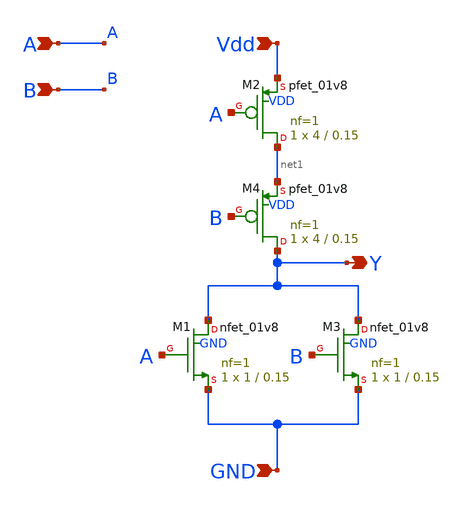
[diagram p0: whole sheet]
** sch_path: 2/src/norlab.sch
**.subckt norlab Y GND A Vdd B
*.opin Y
*.ipin GND
*.ipin A
*.ipin Vdd
*.ipin B
XM1 Y A GND GND sky130_fd_pr__nfet_01v8 L=0.15 W=1 nf=1 ad='int((1 + 1)/2) * 1 / 1 * 0.29' as='int((1 + 2)/2) * 1 / 1 * 0.29'
+ pd='2*int((1 + 1)/2) * (1 / 1 + 0.29)' ps='2*int((1 + 2)/2) * (1 / 1 + 0.29)' nrd='0.29 / 1 ' nrs='0.29 / 1 '
+ sa=0 sb=0 sd=0 mult=1 m=1
XM2 net1 A Vdd VDD sky130_fd_pr__pfet_01v8 L=0.15 W=4 nf=1 ad='int((1 + 1)/2) * 4 / 1 * 0.29' as='int((1 + 2)/2) * 4 / 1 * 0.29'
+ pd='2*int((1 + 1)/2) * (4 / 1 + 0.29)' ps='2*int((1 + 2)/2) * (4 / 1 + 0.29)' nrd='0.29 / 4 ' nrs='0.29 / 4 '
+ sa=0 sb=0 sd=0 mult=1 m=1
XM3 Y B GND GND sky130_fd_pr__nfet_01v8 L=0.15 W=1 nf=1 ad='int((1 + 1)/2) * 1 / 1 * 0.29' as='int((1 + 2)/2) * 1 / 1 * 0.29'
+ pd='2*int((1 + 1)/2) * (1 / 1 + 0.29)' ps='2*int((1 + 2)/2) * (1 / 1 + 0.29)' nrd='0.29 / 1 ' nrs='0.29 / 1 '
+ sa=0 sb=0 sd=0 mult=1 m=1
XM4 Y B net1 VDD sky130_fd_pr__pfet_01v8 L=0.15 W=4 nf=1 ad='int((1 + 1)/2) * 4 / 1 * 0.29' as='int((1 + 2)/2) * 4 / 1 * 0.29'
+ pd='2*int((1 + 1)/2) * (4 / 1 + 0.29)' ps='2*int((1 + 2)/2) * (4 / 1 + 0.29)' nrd='0.29 / 4 ' nrs='0.29 / 4 '
+ sa=0 sb=0 sd=0 mult=1 m=1
**.ends
.end
